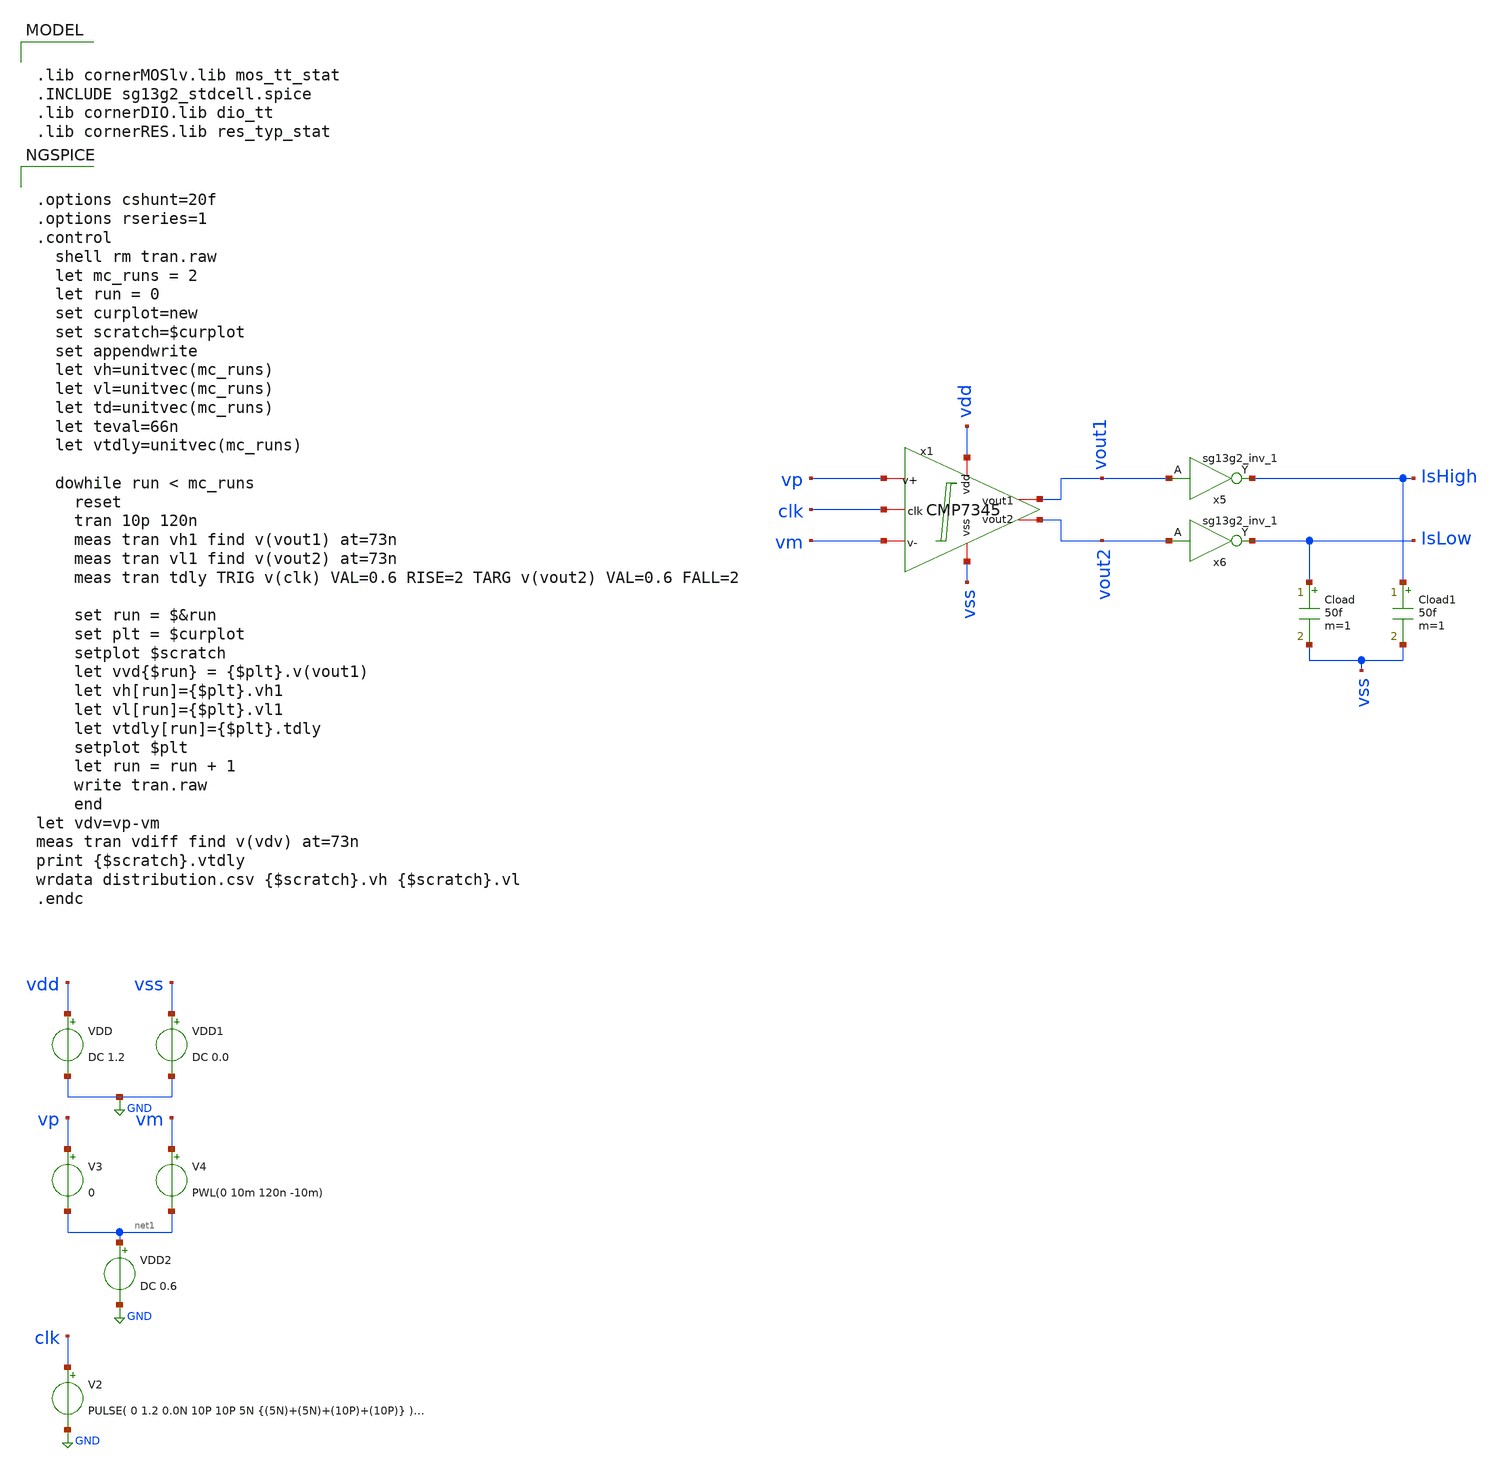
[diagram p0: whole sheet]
** sch_path: CMP7345-main/testbenches/tran/xschem/CMP7345_process_tb.sch
**.subckt CMP7345_process_tb
VDD vdd GND DC 1.2
Cload IsLow vss 50f m=1
x1 vdd vout1 vout2 vp vm clk vss CMP7345
VDD1 vss GND DC 0.0
Cload1 IsHigh vss 50f m=1
V2 clk GND PULSE( 0 1.2 0.0N 10P 10P 5N {(5N)+(5N)+(10P)+(10P)} ) AC 0
V3 vp net1 0
VDD2 net1 GND DC 0.6
x5 IsHigh vout1 VDD VSS sg13g2_inv_1
x6 IsLow vout2 VDD VSS sg13g2_inv_1
V4 vm net1 PWL(0 10m 120n -10m)
**** begin user architecture code

.lib cornerMOSlv.lib mos_tt_stat
.INCLUDE sg13g2_stdcell.spice
.lib cornerDIO.lib dio_tt
.lib cornerRES.lib res_typ_stat



.options cshunt=20f
.options rseries=1
.control
  shell rm tran.raw
  let mc_runs = 2
  let run = 0
  set curplot=new
  set scratch=$curplot
  set appendwrite
  let vh=unitvec(mc_runs)
  let vl=unitvec(mc_runs)
  let td=unitvec(mc_runs)
  let teval=66n
  let vtdly=unitvec(mc_runs)

  dowhile run < mc_runs
    reset
    tran 10p 120n
    meas tran vh1 find v(vout1) at=73n
    meas tran vl1 find v(vout2) at=73n
    meas tran tdly TRIG v(clk) VAL=0.6 RISE=2 TARG v(vout2) VAL=0.6 FALL=2

    set run = $&run
    set plt = $curplot
    setplot $scratch
    let vvd{$run} = {$plt}.v(vout1)
    let vh[run]={$plt}.vh1
    let vl[run]={$plt}.vl1
    let vtdly[run]={$plt}.tdly
    setplot $plt
    let run = run + 1
    write tran.raw
    end
let vdv=vp-vm
meas tran vdiff find v(vdv) at=73n
print {$scratch}.vtdly
wrdata distribution.csv {$scratch}.vh {$scratch}.vl
.endc


**** end user architecture code
**.ends

* expanding   symbol:  sg13g2_stdcells/sg13g2_inv_1.sym # of pins=2
** sym_path: sg13g2_stdcells/sg13g2_inv_1.sym
** sch_path: sg13g2_stdcells/sg13g2_inv_1.sch
.subckt sg13g2_inv_1 Y A VDD VSS
*.opin Y
*.ipin A
*.iopin VDD
*.iopin VSS
XM1 Y A VSS VSS sg13_lv_nmos w=740.00n l=130.00n ng=1 m=1 mm_ok=1
XM2 Y A VDD VDD sg13_lv_pmos w=1.12u l=130.00n ng=1 m=1 mm_ok=1
.ends

.GLOBAL GND
.end
